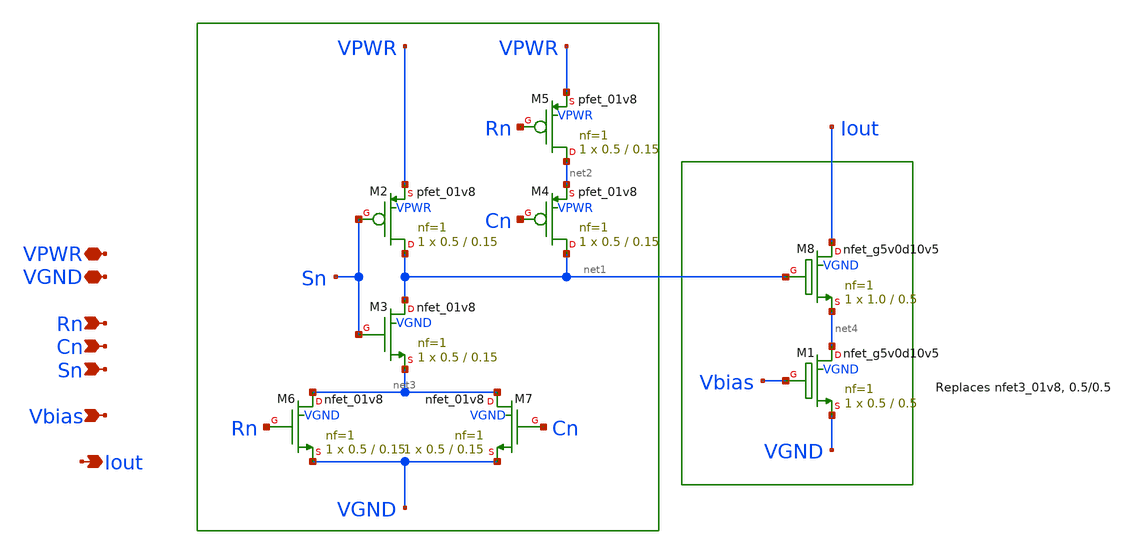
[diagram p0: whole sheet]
** sch_path: xschem/icell.sch
**.subckt icell Rn VPWR Iout VGND Cn Sn Vbias
*.ipin Rn
*.iopin VPWR
*.opin Iout
*.iopin VGND
*.ipin Cn
*.ipin Sn
*.ipin Vbias
XM2 net1 Sn VPWR VPWR sky130_fd_pr__pfet_01v8 L=0.15 W=0.5 nf=1 ad='int((nf+1)/2) * W/nf * 0.29' as='int((nf+2)/2) * W/nf * 0.29'
+ pd='2*int((nf+1)/2) * (W/nf + 0.29)' ps='2*int((nf+2)/2) * (W/nf + 0.29)' nrd='0.29 / W' nrs='0.29 / W'
+ sa=0 sb=0 sd=0 mult=1 m=1
XM3 net1 Sn net3 VGND sky130_fd_pr__nfet_01v8 L=0.15 W=0.5 nf=1 ad='int((nf+1)/2) * W/nf * 0.29' as='int((nf+2)/2) * W/nf * 0.29'
+ pd='2*int((nf+1)/2) * (W/nf + 0.29)' ps='2*int((nf+2)/2) * (W/nf + 0.29)' nrd='0.29 / W' nrs='0.29 / W'
+ sa=0 sb=0 sd=0 mult=1 m=1
XM4 net1 Cn net2 VPWR sky130_fd_pr__pfet_01v8 L=0.15 W=0.5 nf=1 ad='int((nf+1)/2) * W/nf * 0.29' as='int((nf+2)/2) * W/nf * 0.29'
+ pd='2*int((nf+1)/2) * (W/nf + 0.29)' ps='2*int((nf+2)/2) * (W/nf + 0.29)' nrd='0.29 / W' nrs='0.29 / W'
+ sa=0 sb=0 sd=0 mult=1 m=1
XM5 net2 Rn VPWR VPWR sky130_fd_pr__pfet_01v8 L=0.15 W=0.5 nf=1 ad='int((nf+1)/2) * W/nf * 0.29' as='int((nf+2)/2) * W/nf * 0.29'
+ pd='2*int((nf+1)/2) * (W/nf + 0.29)' ps='2*int((nf+2)/2) * (W/nf + 0.29)' nrd='0.29 / W' nrs='0.29 / W'
+ sa=0 sb=0 sd=0 mult=1 m=1
XM6 net3 Rn VGND VGND sky130_fd_pr__nfet_01v8 L=0.15 W=0.5 nf=1 ad='int((nf+1)/2) * W/nf * 0.29' as='int((nf+2)/2) * W/nf * 0.29'
+ pd='2*int((nf+1)/2) * (W/nf + 0.29)' ps='2*int((nf+2)/2) * (W/nf + 0.29)' nrd='0.29 / W' nrs='0.29 / W'
+ sa=0 sb=0 sd=0 mult=1 m=1
XM7 net3 Cn VGND VGND sky130_fd_pr__nfet_01v8 L=0.15 W=0.5 nf=1 ad='int((nf+1)/2) * W/nf * 0.29' as='int((nf+2)/2) * W/nf * 0.29'
+ pd='2*int((nf+1)/2) * (W/nf + 0.29)' ps='2*int((nf+2)/2) * (W/nf + 0.29)' nrd='0.29 / W' nrs='0.29 / W'
+ sa=0 sb=0 sd=0 mult=1 m=1
XM1 net4 Vbias VGND VGND sky130_fd_pr__nfet_g5v0d10v5 L=0.5 W=0.5 nf=1 ad='int((nf+1)/2) * W/nf * 0.29'
+ as='int((nf+2)/2) * W/nf * 0.29' pd='2*int((nf+1)/2) * (W/nf + 0.29)' ps='2*int((nf+2)/2) * (W/nf + 0.29)'
+ nrd='0.29 / W' nrs='0.29 / W' sa=0 sb=0 sd=0 mult=1 m=1
XM8 Iout net1 net4 VGND sky130_fd_pr__nfet_g5v0d10v5 L=0.5 W=1.0 nf=1 ad='int((nf+1)/2) * W/nf * 0.29'
+ as='int((nf+2)/2) * W/nf * 0.29' pd='2*int((nf+1)/2) * (W/nf + 0.29)' ps='2*int((nf+2)/2) * (W/nf + 0.29)'
+ nrd='0.29 / W' nrs='0.29 / W' sa=0 sb=0 sd=0 mult=1 m=1
**.ends
.end
